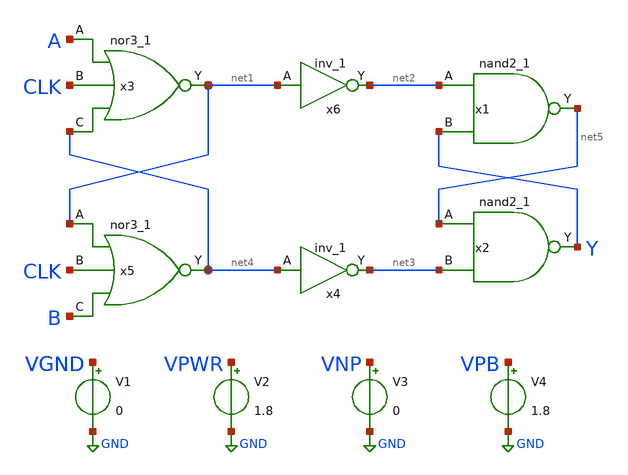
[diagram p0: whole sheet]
** sch_path: analog comparator/nor3-based_comp/schematics/nor3_comp.sch
**.subckt nor3_comp
x1 net2 Y VGND VNB VPB VPWR net5 sky130_fd_sc_hd__nand2_1
x2 net5 net3 VGND VNB VPB VPWR Y sky130_fd_sc_hd__nand2_1
x3 A CLK net4 VGND VNB VPB VPWR net1 sky130_fd_sc_hd__nor3_1
x5 net1 CLK B VGND VNB VPB VPWR net4 sky130_fd_sc_hd__nor3_1
x6 net1 VGND VNB VPB VPWR net2 sky130_fd_sc_hd__inv_1
x4 net4 VGND VNB VPB VPWR net3 sky130_fd_sc_hd__inv_1
V1 VGND GND 0
V2 VPWR GND 1.8
V3 VNP GND 0
V4 VPB GND 1.8
**.ends
.GLOBAL GND
.end
